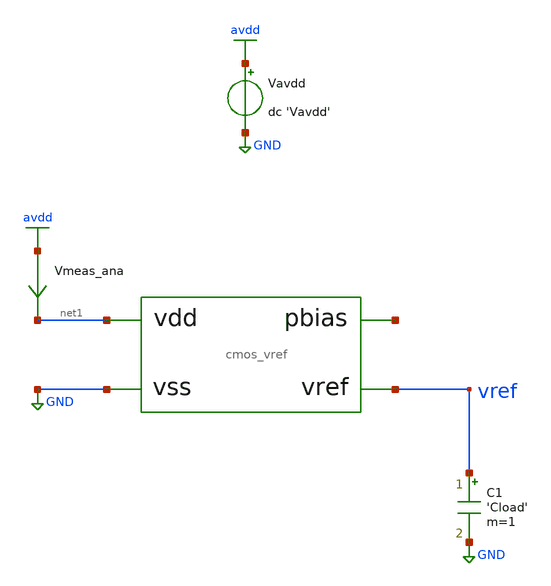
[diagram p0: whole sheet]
** sch_path: tb/cmos_vref/tb_vref_mismatch.sch
**.subckt tb_vref_mismatch
Vavdd avdd GND dc 'Vavdd'
C1 vref GND 'Cload' m=1
Vmeas_ana avdd net1 0
.save i(vmeas_ana)
X1 vref net1 GND net2 cmos_vref
**** begin user architecture code


.lib 'models_dir'/cornerMOShv.lib 'mos_corner'
.lib 'models_dir'/cornerMOSlv.lib 'mos_corner'
.lib 'models_dir'/cornerCAP.lib cap_typ
.option TEMP='temperature'
.option warn=1
.option savecurrents
.control
save all
op
print v(vref) v.x1.vm_b1#branch
set wr_singlescale
wrdata 'simpath'/'filename'_'N'.data v(vref) v.x1.vm_b1#branch
quit
.endc


**** end user architecture code
**.ends
.GLOBAL avdd
.GLOBAL GND
.end
